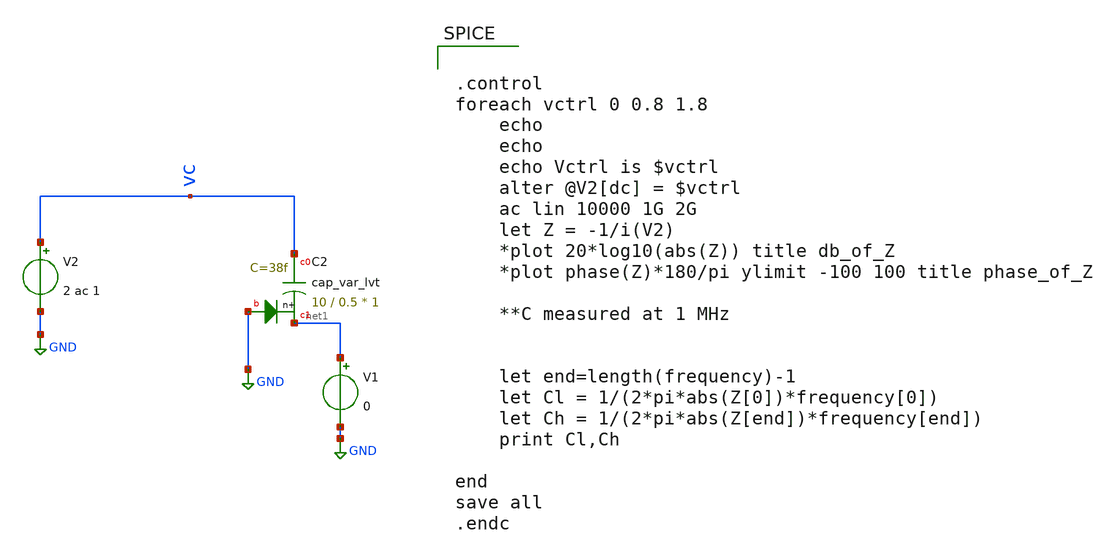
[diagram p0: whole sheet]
** sch_path: varactor_meas/varactor_ac.sch
**.subckt varactor_ac
V2 vc GND 2 ac 1
XC2 vc net1 GND sky130_fd_pr__cap_var_lvt W=10 L=0.5 VM=1 m=1
V1 net1 GND 0
**** begin user architecture code


.control
foreach vctrl 0 0.8 1.8
	echo
	echo
	echo Vctrl is $vctrl
	alter @V2[dc] = $vctrl
	ac lin 10000 1G 2G
	let Z = -1/i(V2)
	*plot 20*log10(abs(Z)) title db_of_Z
	*plot phase(Z)*180/pi ylimit -100 100 title phase_of_Z

	**C measured at 1 MHz


	let end=length(frequency)-1
	let Cl = 1/(2*pi*abs(Z[0])*frequency[0])
	let Ch = 1/(2*pi*abs(Z[end])*frequency[end])
	print Cl,Ch

end
save all
.endc




.option wnflag = 1
.lib /usr/local/share/pdk/sky130A/libs.tech/ngspice/sky130.lib.spice tt
.include /usr/local/share/pdk/sky130A/libs.ref/sky130_fd_pr/spice/sky130_fd_pr__ind_05_220.model.spice
.param mc_mm_switch=0


**** end user architecture code
**.ends
.GLOBAL GND
.end
